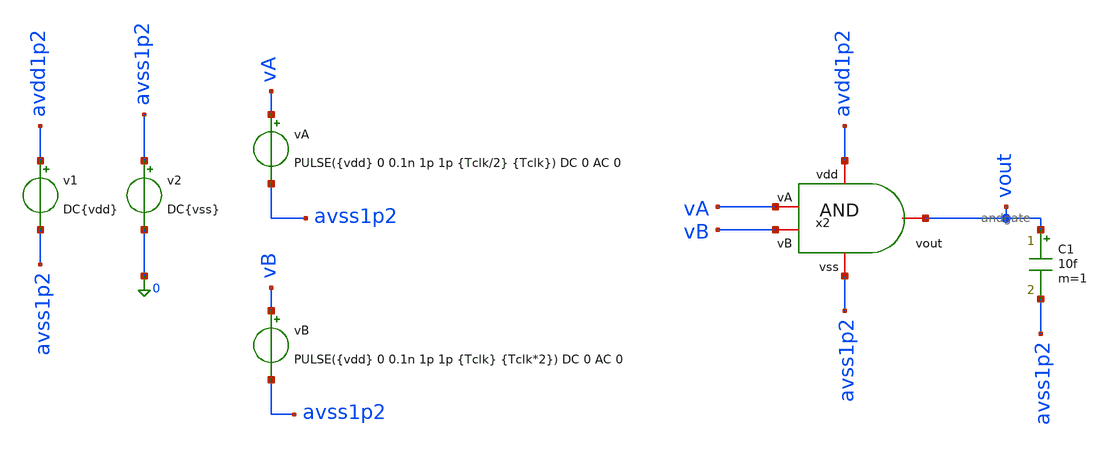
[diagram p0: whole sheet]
** sch_path: design/blocks/testbenches/tb_and.sch
**.subckt tb_and
v1 avdd1p2 avss1p2 DC{vdd}
C1 vout avss1p2 10f m=1
v2 avss1p2 0 DC{vss}
vA vA avss1p2 PULSE({vdd} 0 0.1n 1p 1p {Tclk/2} {Tclk}) DC 0 AC 0
vB vB avss1p2 PULSE({vdd} 0 0.1n 1p 1p {Tclk} {Tclk*2}) DC 0 AC 0
x2 avdd1p2 vB vA vout avss1p2 andgate
**** begin user architecture code


* Circuit Parameters
.param vdd = 1.2
.param vss = 0.0
.param Tclk = 10n
.options TEMP = 27.0
* Include Models - IHP SG13G2
.lib cornerMOSlv.lib mos_tt
* OP Parameters & Singals to save
.save all
*Simulations
.control
tran 0.01u 100n
setplot tran1
plot v(vA) v(vB)+1.5 v(vout)+3
set filetype = ascii
write dcsweep.raw
.endc
.end


**** end user architecture code
**.ends

* expanding   symbol:  blocks/andgate/andgate.sym # of pins=5
** sym_path: design/blocks/andgate/andgate.sym
** sch_path: design/blocks/andgate/andgate.sch
.subckt andgate vdd vA vB vout vss
*.iopin vout
*.iopin vA
*.iopin vB
*.iopin vdd
*.iopin vss
XM2 net1 vA net2 vss sg13_lv_nmos w=1.5u l=0.15u ng=1 m=1 mm_ok=1
XM0 net1 vA vdd vdd sg13_lv_pmos w=1.5u l=0.15u ng=1 m=1 mm_ok=1
XM3 net2 vB vss vss sg13_lv_nmos w=1.5u l=0.15u ng=1 m=1 mm_ok=1
XM1 net1 vB vdd vdd sg13_lv_pmos w=1.5u l=0.15u ng=1 m=1 mm_ok=1
XM4 vout net1 vdd vdd sg13_lv_pmos w=1.5u l=0.15u ng=1 m=1 mm_ok=1
XM5 vout net1 vss vss sg13_lv_nmos w=0.75u l=0.15u ng=1 m=1 mm_ok=1
.ends

.end
